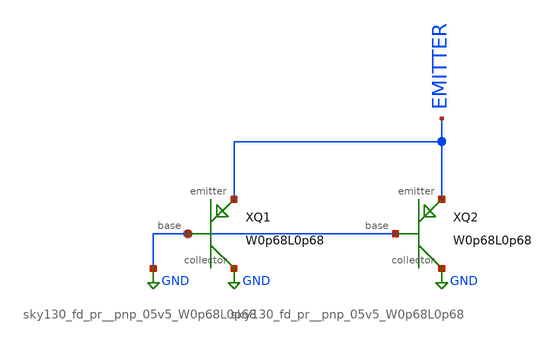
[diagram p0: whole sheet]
** sch_path: projects/pnp/xschem_ngspice/pnp.sch
**.subckt pnp
XQ1 EMITTER GND GND sky130_fd_pr__pnp_05v5_W0p68L0p68
XQ2 EMITTER GND GND sky130_fd_pr__pnp_05v5_W0p68L0p68
**.ends
.GLOBAL GND
.end
